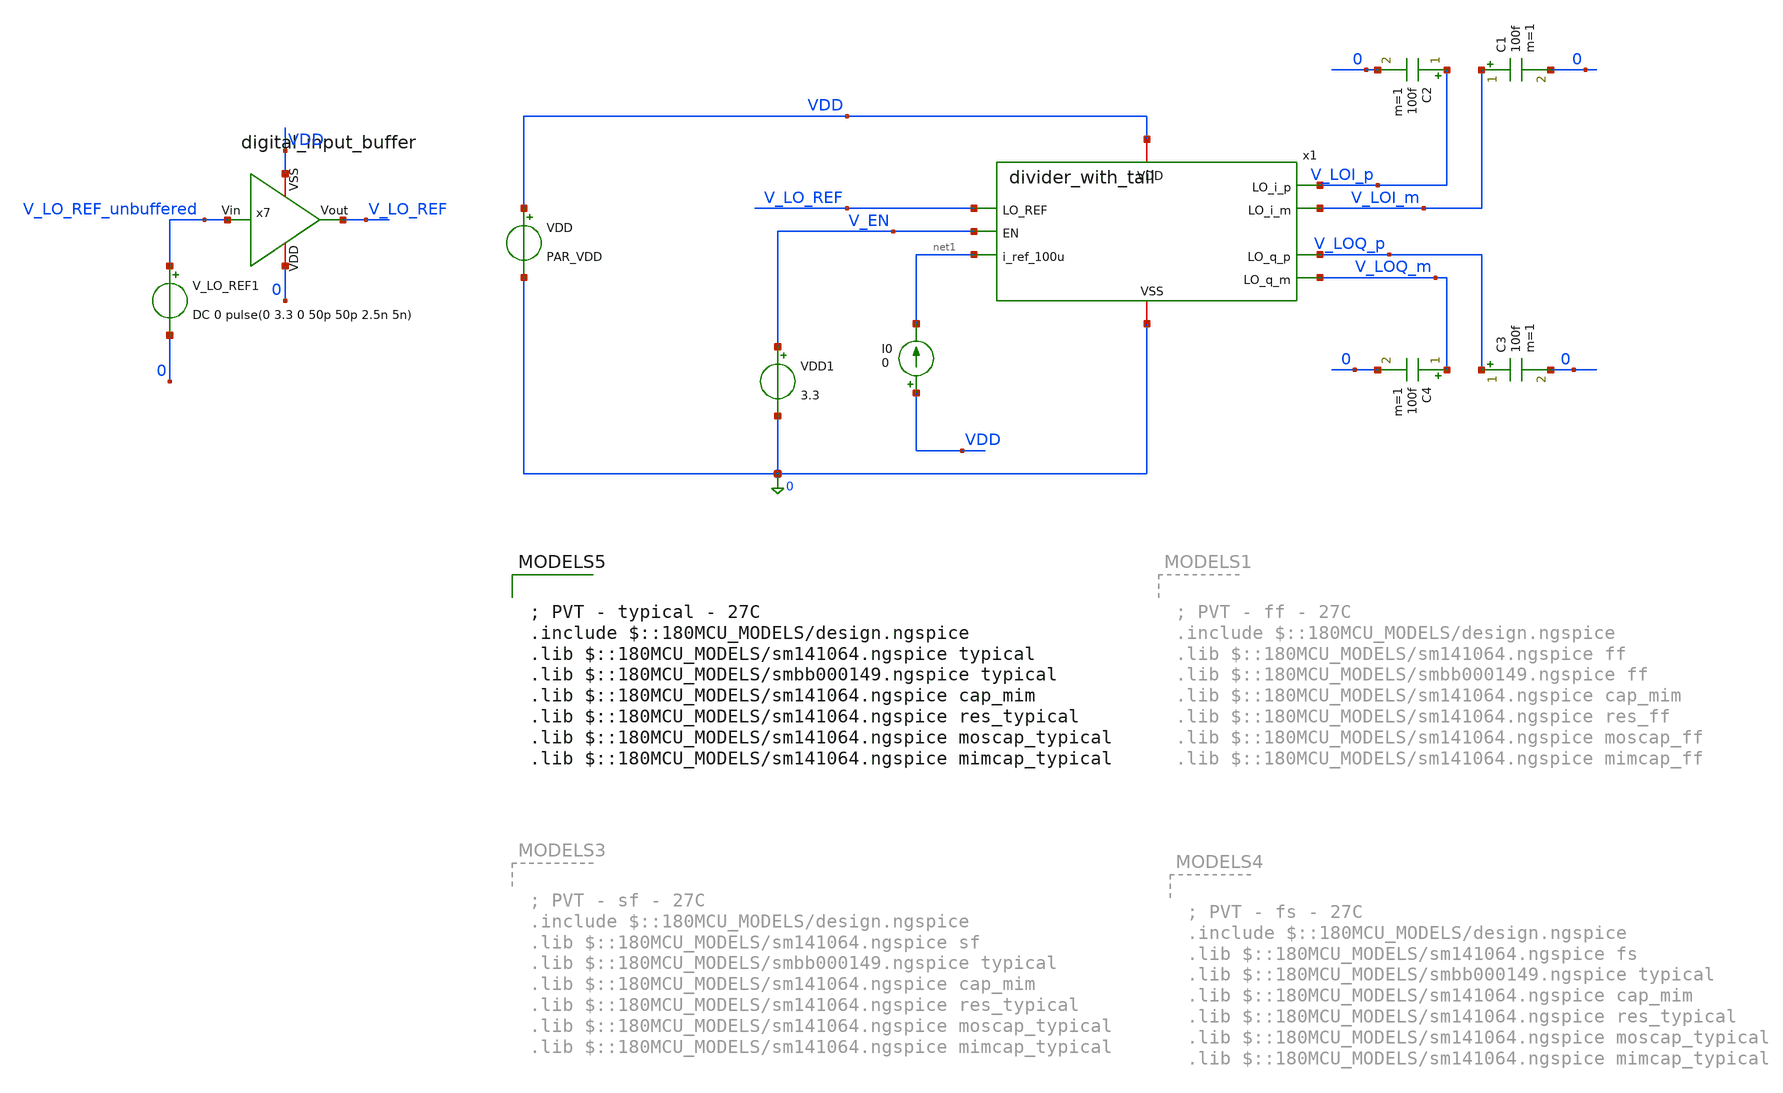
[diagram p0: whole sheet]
** sch_path: designs/divider/testbench/tb_divider_with_tail_pvt.sch
**.subckt tb_divider_with_tail_pvt
VDD VDD 0 PAR_VDD
C1 V_LOI_m 0 100f m=1
C2 V_LOI_p 0 100f m=1
C3 V_LOQ_p 0 100f m=1
C4 V_LOQ_m 0 100f m=1
VDD1 V_EN 0 3.3
V_LO_REF1 V_LO_REF_unbuffered 0 DC 0 pulse(0 3.3 0 50p 50p 2.5n 5n)
x7 VDD V_LO_REF_unbuffered V_LO_REF 0 digital_input_buffer
x1 VDD 0 V_LO_REF V_LOI_p V_LOI_m V_LOQ_p V_LOQ_m V_EN net1 divider_with_tail
I0 VDD net1 0
**** begin user architecture code


** PARAMS

.PARAM PAR_VDD=3.3

.control
destroy all
save all
write tb_divider_with_tail.raw

op
print v(V_LOI_p) v(V_LOI_n)


;transient analysis
tran 0.001n 200n

let V_LOI = v_loi_p - v_loi_m
let V_LOQ = v_loq_p - v_loq_m

plot v(V_LO_REF) v(V_LOI_p)+4 v(V_LOI_m)+4  v(V_LOQ_p)-4 v(V_LOQ_m)-4 ;xlimit 10n 20n;plot divider
+ output
plot v(V_LO_REF) V_LOI+4 V_LOQ+8 ;xlimit 10n 20n; plot differential output
;plot v(V_EN) v(x1.EN_BAR) v(x1.LO_REF_GATED) v(x1.LO_REF_BAR); plot enable signal and clock signal
+ status

plot i(vdd)*3.3 ;transient power

;plot i(v.x1.v1) plot i(v.x1.v2)
;plot v(V_LO_REF) v(x1.LO_REF_BAR)

meas tran t_diff TRIG v(V_LOI) VAL=0 TD=10n RISE=1 TARG v(V_LOQ) VAL=0 TD=10n RISE=1 ; time
+ difference between first rising 0 crossing of V_LOI and first rising 0 cross of V_LOQ after 10ns

;fft of input and output
linearize v(V_LOI) v(v_loq)
fft v(V_LOI) v(v_loq)
plot db(v_loi) db(v_loq) xlimit 1 5G


let V_LOI_MAG = mag(V_LOI)
let V_LOQ_MAG = mag(V_LOQ)
let V_LOI_MAX = maximum(V_LOI_MAG)-0.001; subtract small amount so that meas can find it
meas sp f_har_1 WHEN v(V_LOI_MAG)=V_LOI_MAX; measure first harmonic frequency by measuring frequency
+ of the largest voltage component

;calculate phase error with transient data
let phase_diff_transient = tran1.t_diff * f_har_1 * 360; phase difference = t_diff/t_period = t_diff
+ * f * 360 deg/1
;print phase_diff_transient


;calculate phase error with FFT
let phase_diff_fft = (cph(V_LOI)-cph(V_LOQ))*360/2/pi
meas sp phase_diff_har_1 FIND phase_diff_fft WHEN frequency=f_har_1
;print phase_diff_har_1

echo 'Phase Error with Transient (deg)'
print phase_diff_transient-90
echo 'Phase Error with FFT (deg)'
print phase_diff_har_1-90
echo 'I/Q Amplitude Error (%)'
print (maximum(V_LOQ_MAG)/maximum(V_LOI_MAG)-1)*100

.endc



; PVT - typical - 27C
.include $::180MCU_MODELS/design.ngspice
.lib $::180MCU_MODELS/sm141064.ngspice typical
.lib $::180MCU_MODELS/smbb000149.ngspice typical
.lib $::180MCU_MODELS/sm141064.ngspice cap_mim
.lib $::180MCU_MODELS/sm141064.ngspice res_typical
.lib $::180MCU_MODELS/sm141064.ngspice moscap_typical
.lib $::180MCU_MODELS/sm141064.ngspice mimcap_typical

**** end user architecture code
**.ends
.end
